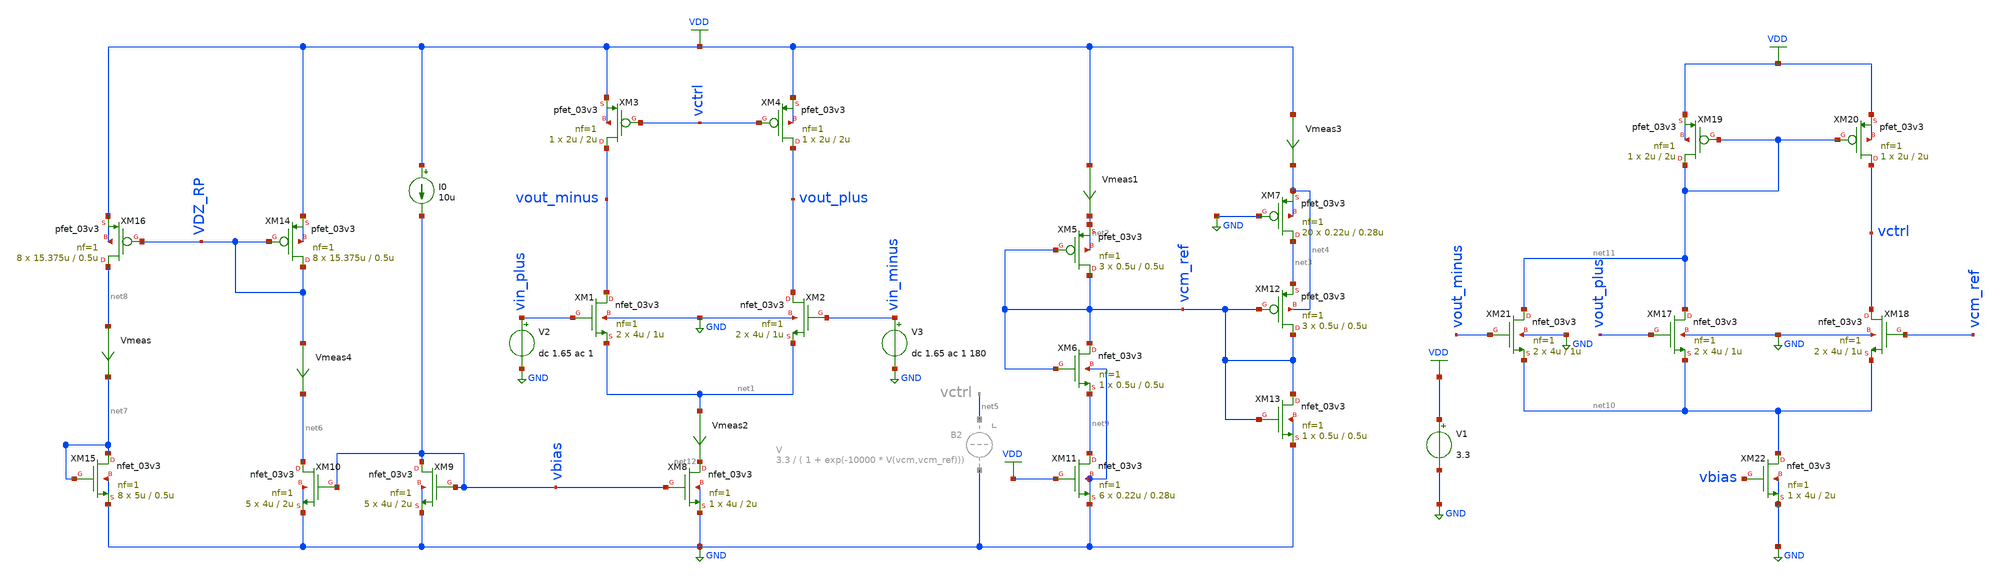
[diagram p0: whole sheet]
** sch_path: Design_Files/Ring-amp/STG1/STG1_fd_AMP.sch
**.subckt STG1_fd_AMP
XM1 vout_minus vin_plus net1 GND nfet_03v3 L=1u W=4u nf=1 ad='int((nf+1)/2) * W/nf * 0.18u' as='int((nf+2)/2) * W/nf * 0.18u'
+ pd='2*int((nf+1)/2) * (W/nf + 0.18u)' ps='2*int((nf+2)/2) * (W/nf + 0.18u)' nrd='0.18u / W' nrs='0.18u / W'
+ sa=0 sb=0 sd=0 m=2
XM2 vout_plus vin_minus net1 GND nfet_03v3 L=1u W=4u nf=1 ad='int((nf+1)/2) * W/nf * 0.18u' as='int((nf+2)/2) * W/nf * 0.18u'
+ pd='2*int((nf+1)/2) * (W/nf + 0.18u)' ps='2*int((nf+2)/2) * (W/nf + 0.18u)' nrd='0.18u / W' nrs='0.18u / W'
+ sa=0 sb=0 sd=0 m=2
XM3 vout_minus vctrl VDD VDD pfet_03v3 L=2u W=2u nf=1 ad='int((nf+1)/2) * W/nf * 0.18u' as='int((nf+2)/2) * W/nf * 0.18u'
+ pd='2*int((nf+1)/2) * (W/nf + 0.18u)' ps='2*int((nf+2)/2) * (W/nf + 0.18u)' nrd='0.18u / W' nrs='0.18u / W'
+ sa=0 sb=0 sd=0 m=1
XM4 vout_plus vctrl VDD VDD pfet_03v3 L=2u W=2u nf=1 ad='int((nf+1)/2) * W/nf * 0.18u' as='int((nf+2)/2) * W/nf * 0.18u'
+ pd='2*int((nf+1)/2) * (W/nf + 0.18u)' ps='2*int((nf+2)/2) * (W/nf + 0.18u)' nrd='0.18u / W' nrs='0.18u / W'
+ sa=0 sb=0 sd=0 m=1
V1 VDD GND 3.3
Vmeas1 VDD net2 0
.save i(vmeas1)
Vmeas3 VDD net4 0
.save i(vmeas3)
V2 vin_plus GND dc 1.65 ac 1
XM8 net12 vbias GND GND nfet_03v3 L=2u W=4u nf=1 ad='int((nf+1)/2) * W/nf * 0.18u' as='int((nf+2)/2) * W/nf * 0.18u'
+ pd='2*int((nf+1)/2) * (W/nf + 0.18u)' ps='2*int((nf+2)/2) * (W/nf + 0.18u)' nrd='0.18u / W' nrs='0.18u / W'
+ sa=0 sb=0 sd=0 m=1
XM9 vbias vbias GND GND nfet_03v3 L=2u W=4u nf=1 ad='int((nf+1)/2) * W/nf * 0.18u' as='int((nf+2)/2) * W/nf * 0.18u'
+ pd='2*int((nf+1)/2) * (W/nf + 0.18u)' ps='2*int((nf+2)/2) * (W/nf + 0.18u)' nrd='0.18u / W' nrs='0.18u / W'
+ sa=0 sb=0 sd=0 m=5
I0 VDD vbias 10u
Vmeas2 net1 net12 0
.save i(vmeas2)
XM10 net6 vbias GND GND nfet_03v3 L=2u W=4u nf=1 ad='int((nf+1)/2) * W/nf * 0.18u' as='int((nf+2)/2) * W/nf * 0.18u'
+ pd='2*int((nf+1)/2) * (W/nf + 0.18u)' ps='2*int((nf+2)/2) * (W/nf + 0.18u)' nrd='0.18u / W' nrs='0.18u / W'
+ sa=0 sb=0 sd=0 m=5
XM14 VDZ_RP VDZ_RP VDD VDD pfet_03v3 L=0.5u W=15.375u nf=1 ad='int((nf+1)/2) * W/nf * 0.18u' as='int((nf+2)/2) * W/nf * 0.18u'
+ pd='2*int((nf+1)/2) * (W/nf + 0.18u)' ps='2*int((nf+2)/2) * (W/nf + 0.18u)' nrd='0.18u / W' nrs='0.18u / W'
+ sa=0 sb=0 sd=0 m=8
Vmeas4 VDZ_RP net6 0
.save i(vmeas4)
XM15 net7 net7 GND GND nfet_03v3 L=0.5u W=5u nf=1 ad='int((nf+1)/2) * W/nf * 0.18u' as='int((nf+2)/2) * W/nf * 0.18u'
+ pd='2*int((nf+1)/2) * (W/nf + 0.18u)' ps='2*int((nf+2)/2) * (W/nf + 0.18u)' nrd='0.18u / W' nrs='0.18u / W'
+ sa=0 sb=0 sd=0 m=8
Vmeas net8 net7 0
.save i(vmeas)
XM16 net8 VDZ_RP VDD VDD pfet_03v3 L=0.5u W=15.375u nf=1 ad='int((nf+1)/2) * W/nf * 0.18u' as='int((nf+2)/2) * W/nf * 0.18u'
+ pd='2*int((nf+1)/2) * (W/nf + 0.18u)' ps='2*int((nf+2)/2) * (W/nf + 0.18u)' nrd='0.18u / W' nrs='0.18u / W'
+ sa=0 sb=0 sd=0 m=8
V3 vin_minus GND dc 1.65 ac 1 180
XM5 vcm_ref vcm_ref net2 net2 pfet_03v3 L=0.5u W=0.5u nf=1 ad='int((nf+1)/2) * W/nf * 0.18u' as='int((nf+2)/2) * W/nf * 0.18u'
+ pd='2*int((nf+1)/2) * (W/nf + 0.18u)' ps='2*int((nf+2)/2) * (W/nf + 0.18u)' nrd='0.18u / W' nrs='0.18u / W'
+ sa=0 sb=0 sd=0 m=3
XM6 vcm_ref vcm_ref net9 GND nfet_03v3 L=0.5u W=0.5u nf=1 ad='int((nf+1)/2) * W/nf * 0.18u' as='int((nf+2)/2) * W/nf * 0.18u'
+ pd='2*int((nf+1)/2) * (W/nf + 0.18u)' ps='2*int((nf+2)/2) * (W/nf + 0.18u)' nrd='0.18u / W' nrs='0.18u / W'
+ sa=0 sb=0 sd=0 m=1
XM11 net9 VDD GND GND nfet_03v3 L=0.28u W=0.22u nf=1 ad='int((nf+1)/2) * W/nf * 0.18u' as='int((nf+2)/2) * W/nf * 0.18u'
+ pd='2*int((nf+1)/2) * (W/nf + 0.18u)' ps='2*int((nf+2)/2) * (W/nf + 0.18u)' nrd='0.18u / W' nrs='0.18u / W'
+ sa=0 sb=0 sd=0 m=6
XM13 vcm_ref vcm_ref GND GND nfet_03v3 L=0.5u W=0.5u nf=1 ad='int((nf+1)/2) * W/nf * 0.18u' as='int((nf+2)/2) * W/nf * 0.18u'
+ pd='2*int((nf+1)/2) * (W/nf + 0.18u)' ps='2*int((nf+2)/2) * (W/nf + 0.18u)' nrd='0.18u / W' nrs='0.18u / W'
+ sa=0 sb=0 sd=0 m=1
XM12 vcm_ref vcm_ref net3 net4 pfet_03v3 L=0.5u W=0.5u nf=1 ad='int((nf+1)/2) * W/nf * 0.18u' as='int((nf+2)/2) * W/nf * 0.18u'
+ pd='2*int((nf+1)/2) * (W/nf + 0.18u)' ps='2*int((nf+2)/2) * (W/nf + 0.18u)' nrd='0.18u / W' nrs='0.18u / W'
+ sa=0 sb=0 sd=0 m=3
XM7 net3 GND net4 net4 pfet_03v3 L=0.28u W=0.22u nf=1 ad='int((nf+1)/2) * W/nf * 0.18u' as='int((nf+2)/2) * W/nf * 0.18u'
+ pd='2*int((nf+1)/2) * (W/nf + 0.18u)' ps='2*int((nf+2)/2) * (W/nf + 0.18u)' nrd='0.18u / W' nrs='0.18u / W'
+ sa=0 sb=0 sd=0 m=20
XM17 net11 vout_plus net10 GND nfet_03v3 L=1u W=4u nf=1 ad='int((nf+1)/2) * W/nf * 0.18u' as='int((nf+2)/2) * W/nf * 0.18u'
+ pd='2*int((nf+1)/2) * (W/nf + 0.18u)' ps='2*int((nf+2)/2) * (W/nf + 0.18u)' nrd='0.18u / W' nrs='0.18u / W'
+ sa=0 sb=0 sd=0 m=2
XM18 vctrl vcm_ref net10 GND nfet_03v3 L=1u W=4u nf=1 ad='int((nf+1)/2) * W/nf * 0.18u' as='int((nf+2)/2) * W/nf * 0.18u'
+ pd='2*int((nf+1)/2) * (W/nf + 0.18u)' ps='2*int((nf+2)/2) * (W/nf + 0.18u)' nrd='0.18u / W' nrs='0.18u / W'
+ sa=0 sb=0 sd=0 m=2
XM19 net11 net11 VDD VDD pfet_03v3 L=2u W=2u nf=1 ad='int((nf+1)/2) * W/nf * 0.18u' as='int((nf+2)/2) * W/nf * 0.18u'
+ pd='2*int((nf+1)/2) * (W/nf + 0.18u)' ps='2*int((nf+2)/2) * (W/nf + 0.18u)' nrd='0.18u / W' nrs='0.18u / W'
+ sa=0 sb=0 sd=0 m=1
XM20 vctrl net11 VDD VDD pfet_03v3 L=2u W=2u nf=1 ad='int((nf+1)/2) * W/nf * 0.18u' as='int((nf+2)/2) * W/nf * 0.18u'
+ pd='2*int((nf+1)/2) * (W/nf + 0.18u)' ps='2*int((nf+2)/2) * (W/nf + 0.18u)' nrd='0.18u / W' nrs='0.18u / W'
+ sa=0 sb=0 sd=0 m=1
XM21 net11 vout_minus net10 GND nfet_03v3 L=1u W=4u nf=1 ad='int((nf+1)/2) * W/nf * 0.18u' as='int((nf+2)/2) * W/nf * 0.18u'
+ pd='2*int((nf+1)/2) * (W/nf + 0.18u)' ps='2*int((nf+2)/2) * (W/nf + 0.18u)' nrd='0.18u / W' nrs='0.18u / W'
+ sa=0 sb=0 sd=0 m=2
XM22 net10 vbias GND GND nfet_03v3 L=2u W=4u nf=1 ad='int((nf+1)/2) * W/nf * 0.18u' as='int((nf+2)/2) * W/nf * 0.18u'
+ pd='2*int((nf+1)/2) * (W/nf + 0.18u)' ps='2*int((nf+2)/2) * (W/nf + 0.18u)' nrd='0.18u / W' nrs='0.18u / W'
+ sa=0 sb=0 sd=0 m=1
**** begin user architecture code


.option wnflag=1
.option savecurrents
.temp 27
.control
save all
write STG1_fd_AMP.raw
set appendwrite
op
write STG1_fd_AMP.raw
**dc V1 0 1.65 1m
**tran 1m 10m 1m
**tran 100n 5u 100n
ac dec 20 1 1e10
plot vdb(vout_plus)
plot vdb(vout_minus)
let vout=v(vout_plus)-v(vout_minus)
plot vdb(vout)
.endc




.save @m.xm1.m0[gm]
.save @m.xm1.m0[id]
.save @m.xm1.m0[vth]
.save @m.xm1.m0[gds]
.save @m.xm1.m0[cgg]
.save @m.xm1.m0[cgs]
.save @m.xm1.m0[cgd]
.save @m.xm2.m0[gm]
.save @m.xm2.m0[id]
.save @m.xm2.m0[vth]
.save @m.xm2.m0[gds]
.save @m.xm2.m0[cgg]
.save @m.xm2.m0[cgs]
.save @m.xm2.m0[cgd]
.save @m.xm3.m0[gm]
.save @m.xm3.m0[id]
.save @m.xm3.m0[vth]
.save @m.xm3.m0[vds]
.save @m.xm3.m0[gds]
.save @m.xm3.m0[cgg]
.save @m.xm3.m0[cgs]
.save @m.xm3.m0[cgd]
.save @m.xm4.m0[gm]
.save @m.xm4.m0[id]
.save @m.xm4.m0[vth]
.save @m.xm4.m0[vds]
.save @m.xm4.m0[gds]
.save @m.xm4.m0[cgg]
.save @m.xm4.m0[cgs]
.save @m.xm4.m0[cgd]



.lib /foss/pdks/volare/gf180mcu/versions/0fe599b2afb6708d281543108caf8310912f54af/gf180mcuD/libs.tech/ngspice/sm141064.ngspice typical
.include /foss/pdks/volare/gf180mcu/versions/0fe599b2afb6708d281543108caf8310912f54af/gf180mcuD/libs.tech/ngspice/design.ngspice
.lib /foss/pdks/volare/gf180mcu/versions/0fe599b2afb6708d281543108caf8310912f54af/gf180mcuD/libs.tech/ngspice/sm141064.ngspice res_statistical

**.include $::180MCU_MODELS/design.ngspice
**.lib $::180MCU_MODELS/sm141064.ngspice typical
**.lib $::180MCU_MODELS/sm141064.ngspice res_typical
* .lib $::180MCU_MODELS/sm141064.ngspice res_statistical
*.include $::180MCU_MODELS/design.ngspice
*.lib $::180MCU_MODELS/sm141064.ngspice typical


**** end user architecture code
**.ends
.GLOBAL VDD
.GLOBAL GND
.end
